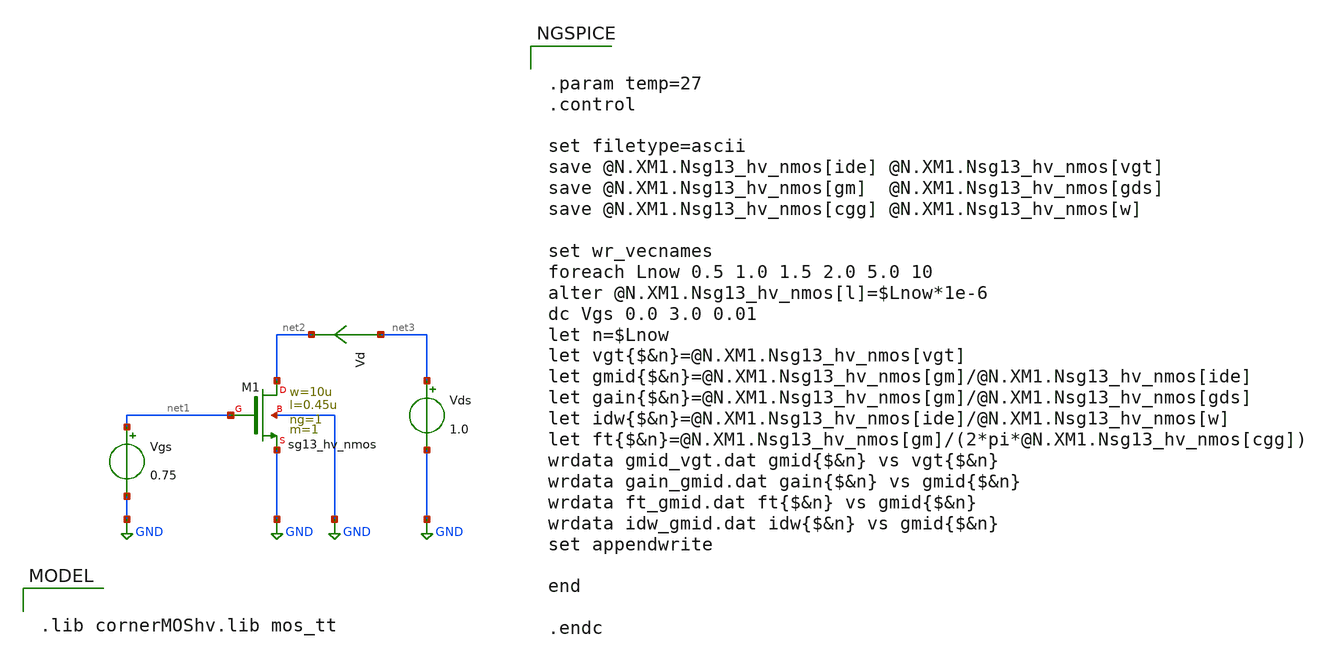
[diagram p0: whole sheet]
** sch_path: gmid_hv_nmos.sch
* Copyright 2023 IHP PDK Authors
**.subckt gmid_hv_nmos
Vgs net1 GND 0.75
Vds net3 GND 1.0
Vd net3 net2 0
.save i(vd)
XM1 net2 net1 GND GND sg13_hv_nmos w=10u l=0.45u ng=1 m=1 mm_ok=1
**** begin user architecture code

.lib cornerMOShv.lib mos_tt



.param temp=27
.control

set filetype=ascii
save @N.XM1.Nsg13_hv_nmos[ide] @N.XM1.Nsg13_hv_nmos[vgt]
save @N.XM1.Nsg13_hv_nmos[gm]  @N.XM1.Nsg13_hv_nmos[gds]
save @N.XM1.Nsg13_hv_nmos[cgg] @N.XM1.Nsg13_hv_nmos[w]

set wr_vecnames
foreach Lnow 0.5 1.0 1.5 2.0 5.0 10
alter @N.XM1.Nsg13_hv_nmos[l]=$Lnow*1e-6
dc Vgs 0.0 3.0 0.01
let n=$Lnow
let vgt{$&n}=@N.XM1.Nsg13_hv_nmos[vgt]
let gmid{$&n}=@N.XM1.Nsg13_hv_nmos[gm]/@N.XM1.Nsg13_hv_nmos[ide]
let gain{$&n}=@N.XM1.Nsg13_hv_nmos[gm]/@N.XM1.Nsg13_hv_nmos[gds]
let idw{$&n}=@N.XM1.Nsg13_hv_nmos[ide]/@N.XM1.Nsg13_hv_nmos[w]
let ft{$&n}=@N.XM1.Nsg13_hv_nmos[gm]/(2*pi*@N.XM1.Nsg13_hv_nmos[cgg])
wrdata gmid_vgt.dat gmid{$&n} vs vgt{$&n}
wrdata gain_gmid.dat gain{$&n} vs gmid{$&n}
wrdata ft_gmid.dat ft{$&n} vs gmid{$&n}
wrdata idw_gmid.dat idw{$&n} vs gmid{$&n}
set appendwrite

end

.endc


**** end user architecture code
**.ends
.GLOBAL GND
.end
